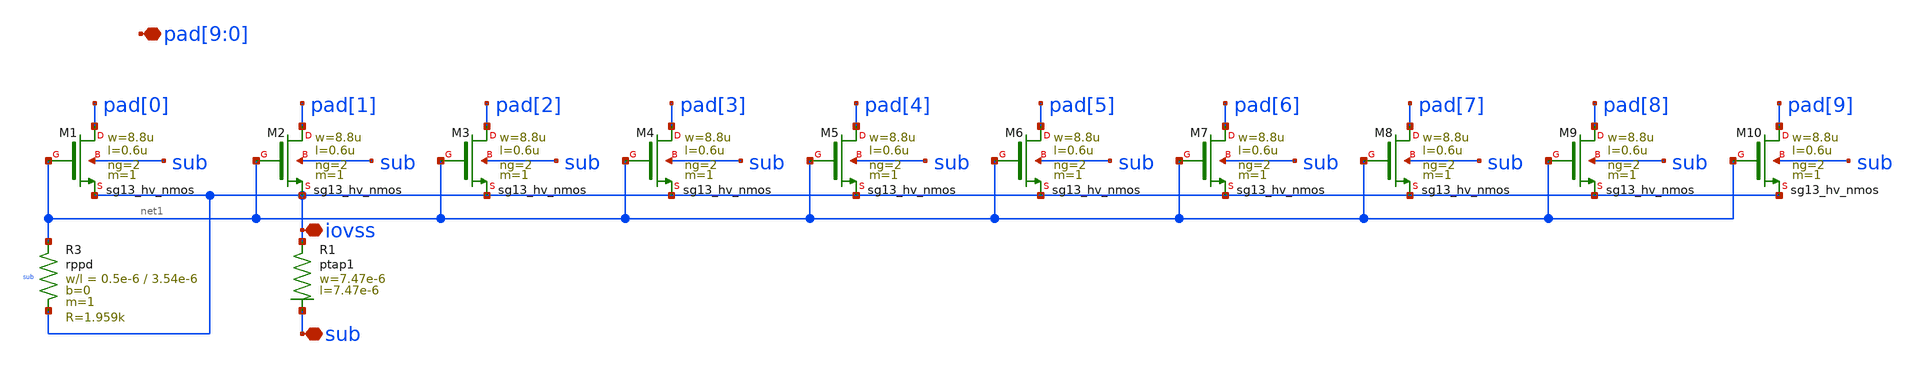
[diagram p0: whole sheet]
** sch_path: MSPHY6034-main/dependencies/unic_cass_2025_team04_padring/xschem/openpdk-libraries/ihp-sg13g2/sg13g2_io/xschem/sg13g2_Clamp_N20N0D.sch
**.subckt sg13g2_Clamp_N20N0D iovss
*+ pad[9],pad[8],pad[7],pad[6],pad[5],pad[4],pad[3],pad[2],pad[1],pad[0] sub
*.iopin iovss
*.iopin pad[9],pad[8],pad[7],pad[6],pad[5],pad[4],pad[3],pad[2],pad[1],pad[0]
*.iopin sub
XR1 iovss sub ptap1 R=11.44 w=7.47e-6 l=7.47e-6
XM1 pad[0] net1 iovss sub sg13_hv_nmos w=8.8u l=0.6u ng=2 m=1 mm_ok=1
XM2 pad[1] net1 iovss sub sg13_hv_nmos w=8.8u l=0.6u ng=2 m=1 mm_ok=1
XM3 pad[2] net1 iovss sub sg13_hv_nmos w=8.8u l=0.6u ng=2 m=1 mm_ok=1
XM4 pad[3] net1 iovss sub sg13_hv_nmos w=8.8u l=0.6u ng=2 m=1 mm_ok=1
XM5 pad[4] net1 iovss sub sg13_hv_nmos w=8.8u l=0.6u ng=2 m=1 mm_ok=1
XM6 pad[5] net1 iovss sub sg13_hv_nmos w=8.8u l=0.6u ng=2 m=1 mm_ok=1
XM7 pad[6] net1 iovss sub sg13_hv_nmos w=8.8u l=0.6u ng=2 m=1 mm_ok=1
XM8 pad[7] net1 iovss sub sg13_hv_nmos w=8.8u l=0.6u ng=2 m=1 mm_ok=1
XM9 pad[8] net1 iovss sub sg13_hv_nmos w=8.8u l=0.6u ng=2 m=1 mm_ok=1
XM10 pad[9] net1 iovss sub sg13_hv_nmos w=8.8u l=0.6u ng=2 m=1 mm_ok=1
XR3 net1 iovss sub rppd w=0.5e-6 l=3.54e-6 m=1 b=0 mm_ok=1
**.ends
.end
